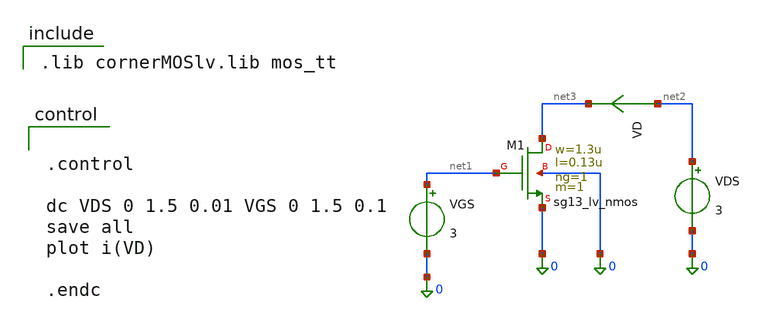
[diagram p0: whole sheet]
** sch_path: designs/nmos.sch
**.subckt nmos
XM1 net3 net1 0 0 sg13_lv_nmos w=1.3u l=0.13u ng=1 m=1 mm_ok=1
VGS net1 0 3
VDS net2 0 3
VD net2 net3 0
.save i(vd)
**** begin user architecture code

.lib cornerMOSlv.lib mos_tt



.control

dc VDS 0 1.5 0.01 VGS 0 1.5 0.1
save all
plot i(VD)

.endc


**** end user architecture code
**.ends
.end
